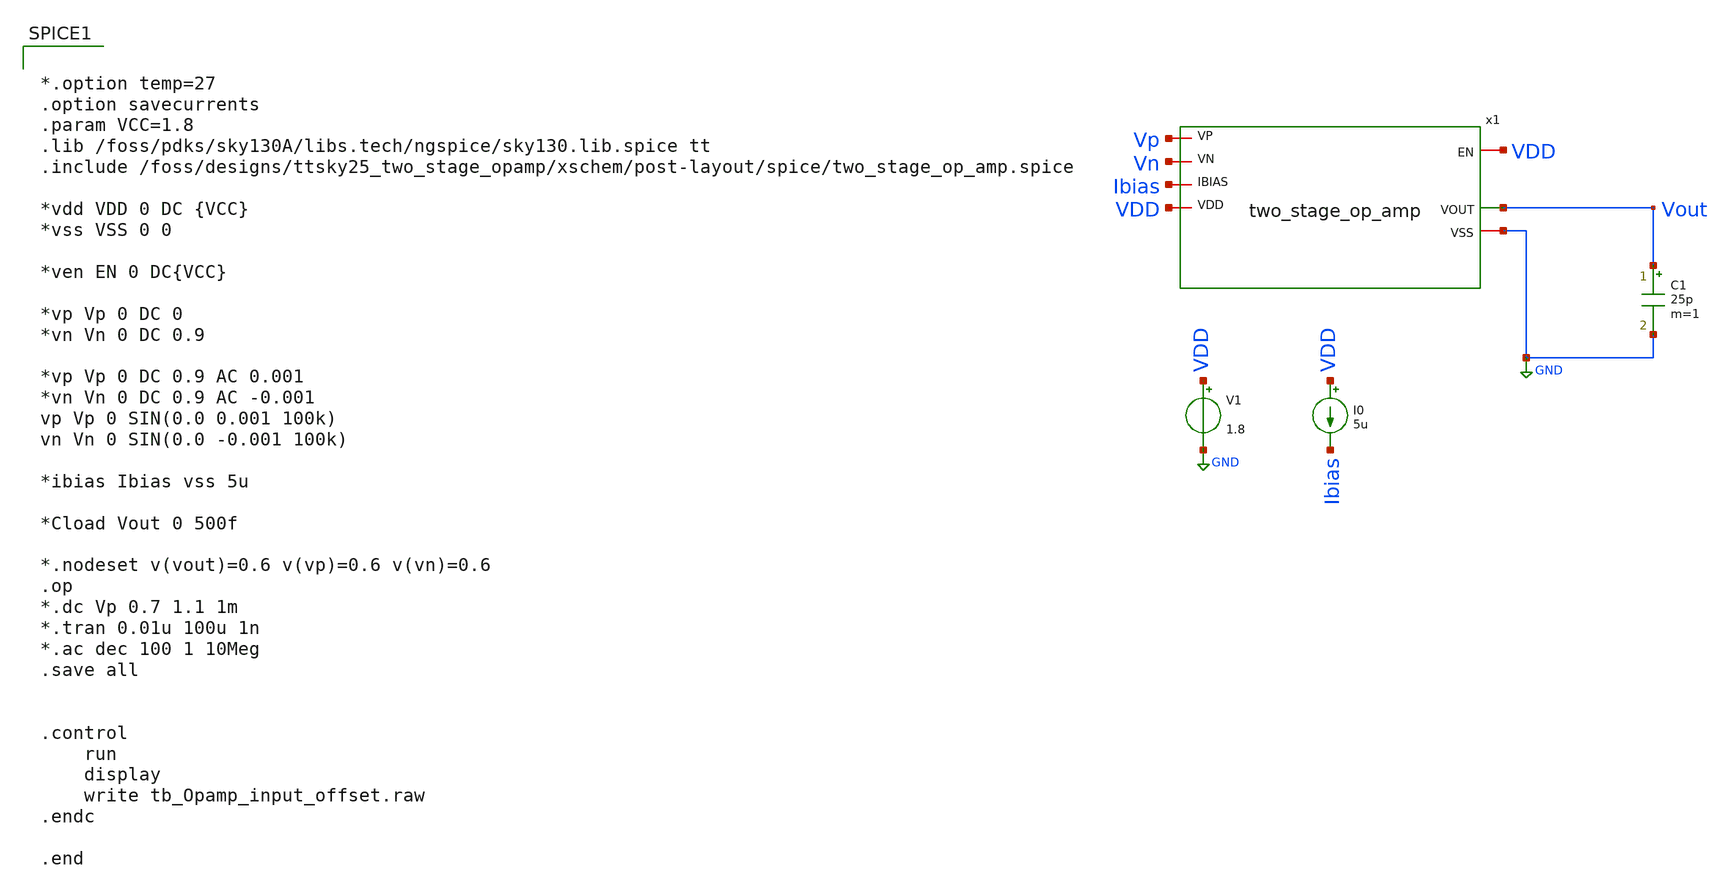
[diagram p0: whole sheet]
** sch_path: xschem/post-layout/testbenches/tb_Opamp_input_offset.sch
**.subckt tb_Opamp_input_offset
V1 VDD GND 1.8
I0 VDD Ibias 5u
C1 Vout GND 25p m=1
x1 VDD GND Ibias Vout Vp Vn VDD two_stage_op_amp
**** begin user architecture code


*.option temp=27
.option savecurrents
.param VCC=1.8
.lib /foss/pdks/sky130A/libs.tech/ngspice/sky130.lib.spice tt
.include /foss/designs/ttsky25_two_stage_opamp/xschem/post-layout/spice/two_stage_op_amp.spice

*vdd VDD 0 DC {VCC}
*vss VSS 0 0

*ven EN 0 DC{VCC}

*vp Vp 0 DC 0
*vn Vn 0 DC 0.9

*vp Vp 0 DC 0.9 AC 0.001
*vn Vn 0 DC 0.9 AC -0.001
vp Vp 0 SIN(0.0 0.001 100k)
vn Vn 0 SIN(0.0 -0.001 100k)

*ibias Ibias vss 5u

*Cload Vout 0 500f

*.nodeset v(vout)=0.6 v(vp)=0.6 v(vn)=0.6
.op
*.dc Vp 0.7 1.1 1m
*.tran 0.01u 100u 1n
*.ac dec 100 1 10Meg
.save all


.control
	run
	display
	write tb_Opamp_input_offset.raw
.endc

.end


**** end user architecture code
**.ends
.GLOBAL GND
.end
